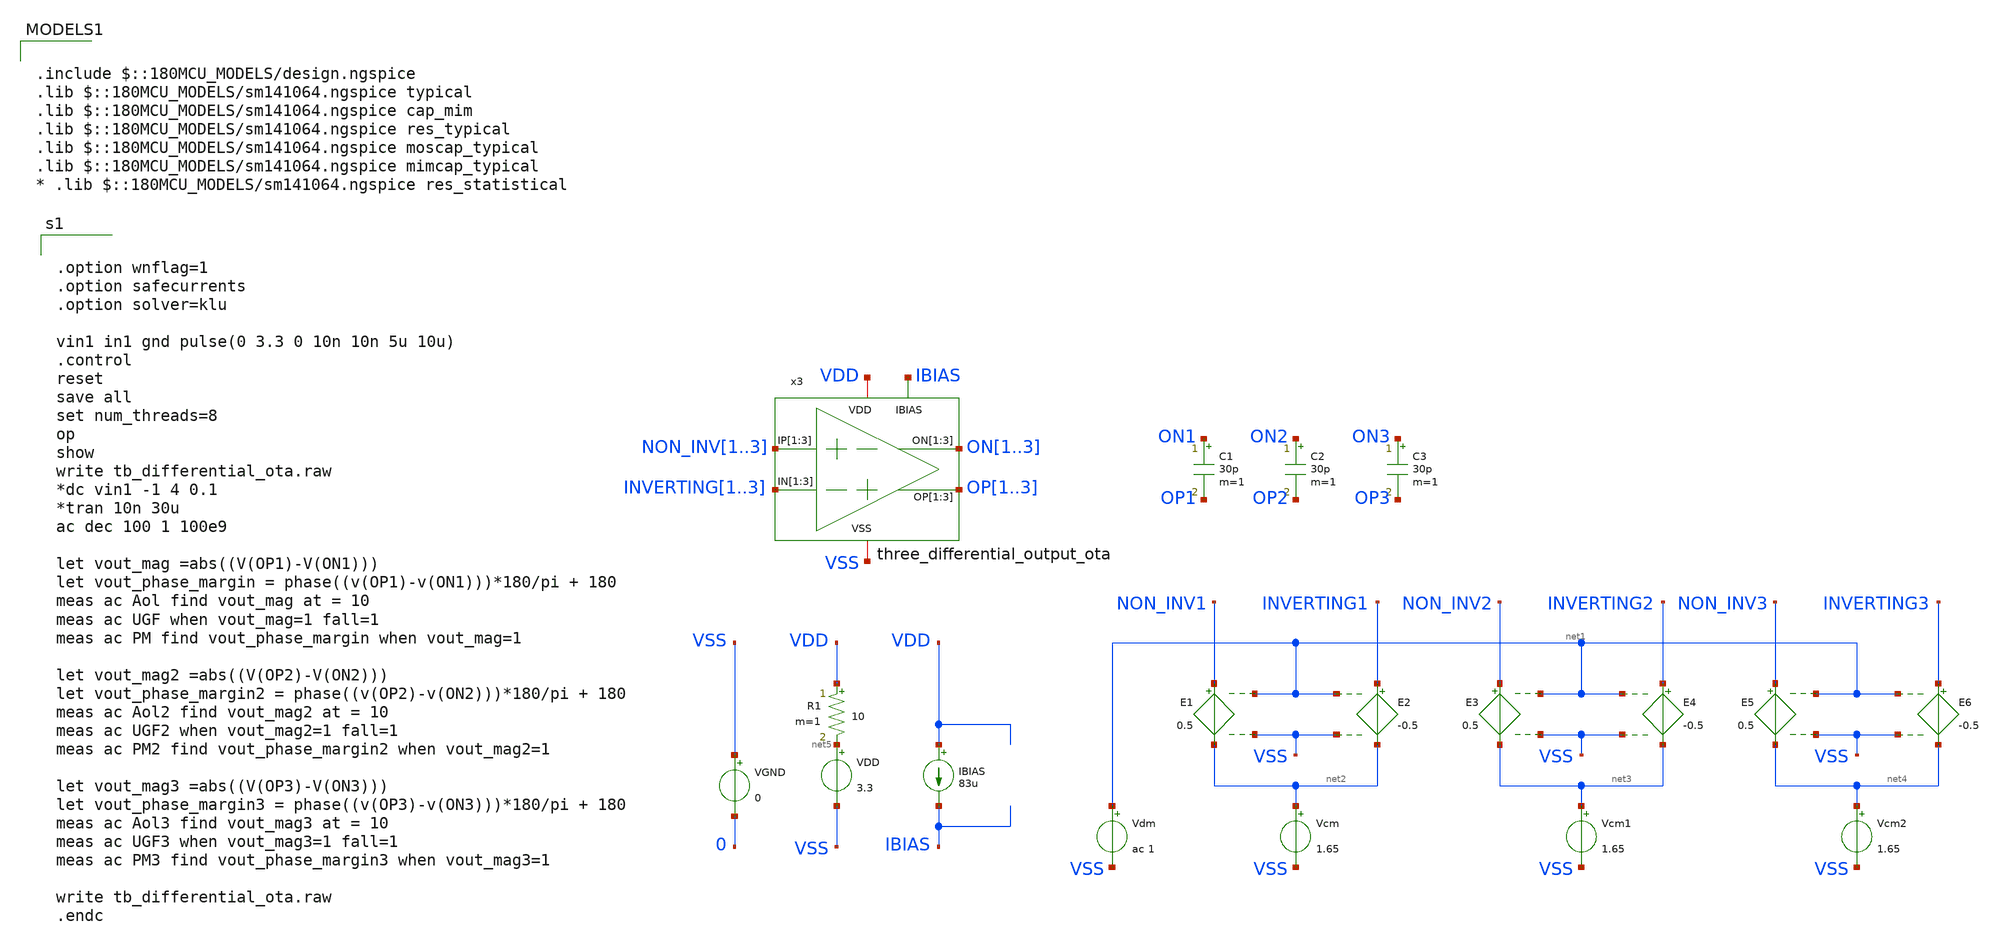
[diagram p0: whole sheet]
** sch_path: designs/libs/tb_ota/tb_three_differential_output_ota/tb_differential_ota.sch
**.subckt tb_differential_ota
E1 NON_INV1 net2 net1 VSS 0.5
E2 INVERTING1 net2 net1 VSS -0.5
Vdm net1 VSS ac 1
Vcm net2 VSS 1.65
VDD net5 VSS 3.3
R1 VDD net5 10 m=1
IBIAS VDD IBIAS 83u
VGND VSS 0 0
C1 ON1 OP1 30p m=1
x3 NON_INV1 NON_INV2 NON_INV3 INVERTING1 INVERTING2 INVERTING3 IBIAS OP1 OP2 OP3 VDD VSS ON1 ON2 ON3
+ three_differential_output_ota
E3 NON_INV2 net3 net1 VSS 0.5
E4 INVERTING2 net3 net1 VSS -0.5
Vcm1 net3 VSS 1.65
E5 NON_INV3 net4 net1 VSS 0.5
E6 INVERTING3 net4 net1 VSS -0.5
Vcm2 net4 VSS 1.65
C2 ON2 OP2 30p m=1
C3 ON3 OP3 30p m=1
**** begin user architecture code


.option wnflag=1
.option safecurrents
.option solver=klu

vin1 in1 gnd pulse(0 3.3 0 10n 10n 5u 10u)
.control
reset
save all
set num_threads=8
op
show
write tb_differential_ota.raw
*dc vin1 -1 4 0.1
*tran 10n 30u
ac dec 100 1 100e9

let vout_mag =abs((V(OP1)-V(ON1)))
let vout_phase_margin = phase((v(OP1)-v(ON1)))*180/pi + 180
meas ac Aol find vout_mag at = 10
meas ac UGF when vout_mag=1 fall=1
meas ac PM find vout_phase_margin when vout_mag=1

let vout_mag2 =abs((V(OP2)-V(ON2)))
let vout_phase_margin2 = phase((v(OP2)-v(ON2)))*180/pi + 180
meas ac Aol2 find vout_mag2 at = 10
meas ac UGF2 when vout_mag2=1 fall=1
meas ac PM2 find vout_phase_margin2 when vout_mag2=1

let vout_mag3 =abs((V(OP3)-V(ON3)))
let vout_phase_margin3 = phase((v(OP3)-v(ON3)))*180/pi + 180
meas ac Aol3 find vout_mag3 at = 10
meas ac UGF3 when vout_mag3=1 fall=1
meas ac PM3 find vout_phase_margin3 when vout_mag3=1

write tb_differential_ota.raw
.endc



.include $::180MCU_MODELS/design.ngspice
.lib $::180MCU_MODELS/sm141064.ngspice typical
.lib $::180MCU_MODELS/sm141064.ngspice cap_mim
.lib $::180MCU_MODELS/sm141064.ngspice res_typical
.lib $::180MCU_MODELS/sm141064.ngspice moscap_typical
.lib $::180MCU_MODELS/sm141064.ngspice mimcap_typical
* .lib $::180MCU_MODELS/sm141064.ngspice res_statistical

**** end user architecture code
**.ends
.end
